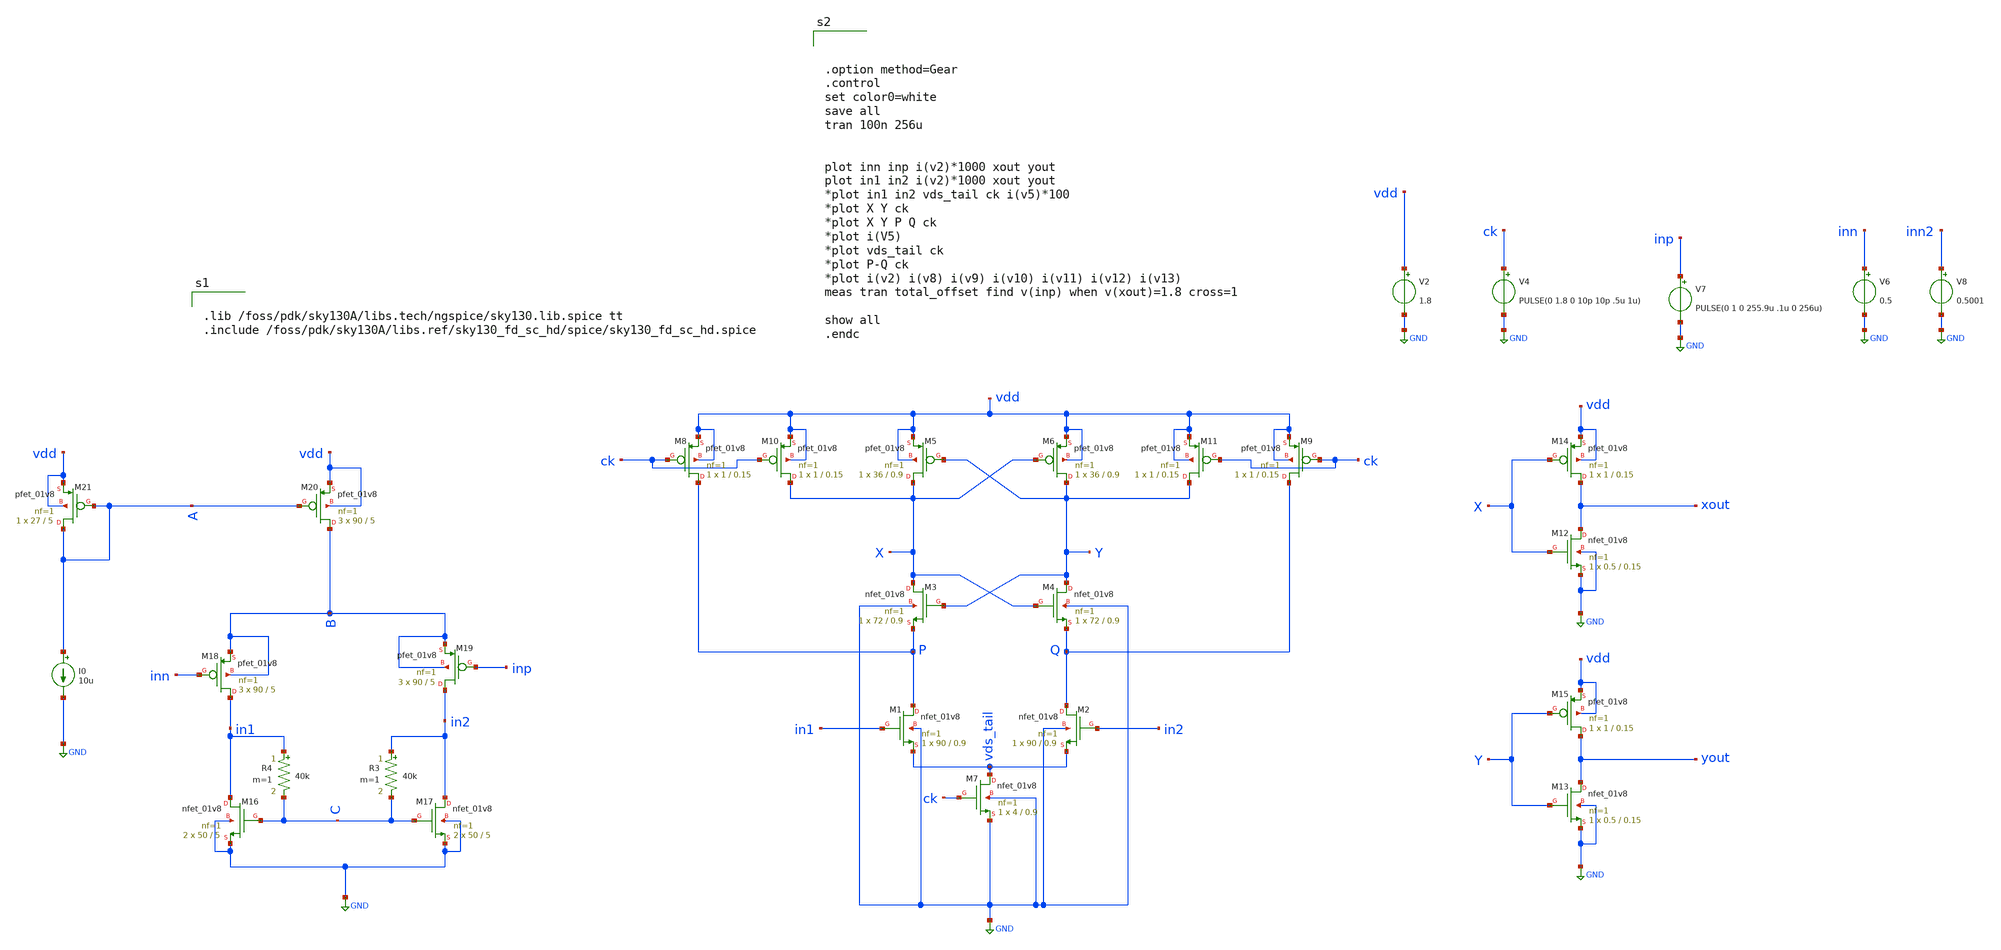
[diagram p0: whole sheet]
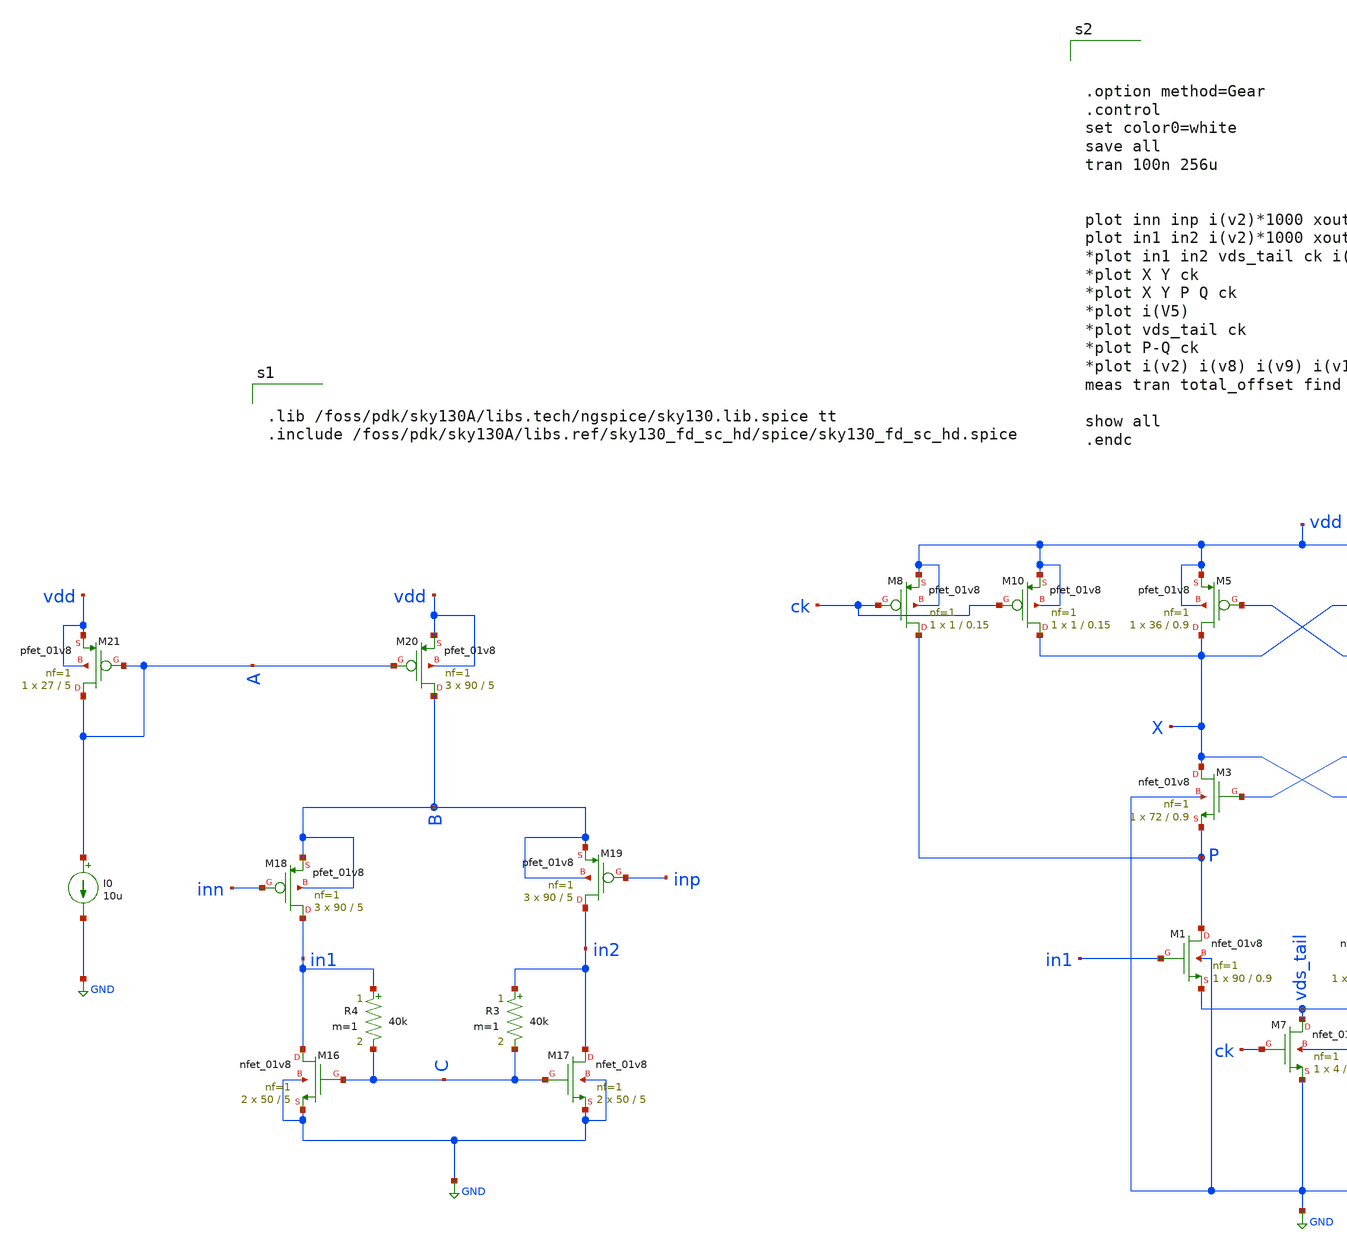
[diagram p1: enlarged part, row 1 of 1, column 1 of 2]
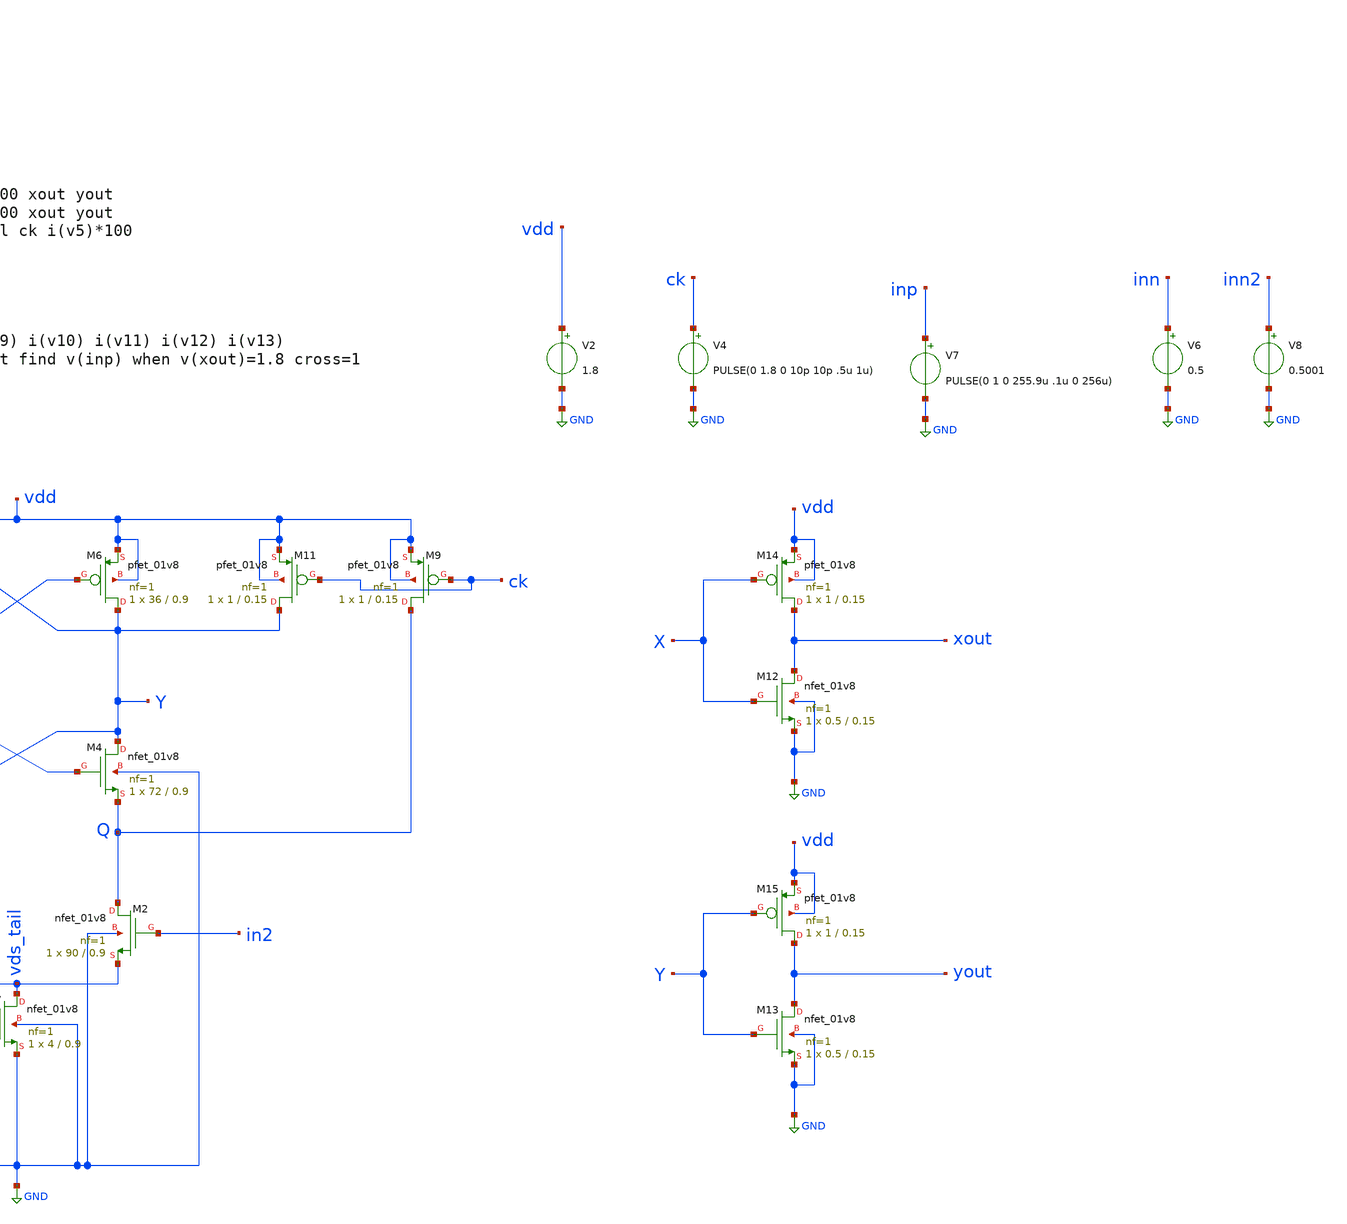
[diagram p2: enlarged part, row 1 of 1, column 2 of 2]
** sch_path: analog/lib/comp_with_preamp_large_new.sch
**.subckt comp_with_preamp_large_new
XM10 X ck vdd vdd sky130_fd_pr__pfet_01v8 L=0.15 W=1 nf=1 ad='int((nf+1)/2) * W/nf * 0.29' as='int((nf+2)/2) * W/nf * 0.29'
+ pd='2*int((nf+1)/2) * (W/nf + 0.29)' ps='2*int((nf+2)/2) * (W/nf + 0.29)' nrd='0.29 / W' nrs='0.29 / W'
+ sa=0 sb=0 sd=0 mult=1 m=1
XM8 P ck vdd vdd sky130_fd_pr__pfet_01v8 L=0.15 W=1 nf=1 ad='int((nf+1)/2) * W/nf * 0.29' as='int((nf+2)/2) * W/nf * 0.29'
+ pd='2*int((nf+1)/2) * (W/nf + 0.29)' ps='2*int((nf+2)/2) * (W/nf + 0.29)' nrd='0.29 / W' nrs='0.29 / W'
+ sa=0 sb=0 sd=0 mult=1 m=1
XM5 X Y vdd vdd sky130_fd_pr__pfet_01v8 L=0.9 W=36 nf=1 ad='int((nf+1)/2) * W/nf * 0.29' as='int((nf+2)/2) * W/nf * 0.29'
+ pd='2*int((nf+1)/2) * (W/nf + 0.29)' ps='2*int((nf+2)/2) * (W/nf + 0.29)' nrd='0.29 / W' nrs='0.29 / W'
+ sa=0 sb=0 sd=0 mult=1 m=1
XM6 Y X vdd vdd sky130_fd_pr__pfet_01v8 L=0.9 W=36 nf=1 ad='int((nf+1)/2) * W/nf * 0.29' as='int((nf+2)/2) * W/nf * 0.29'
+ pd='2*int((nf+1)/2) * (W/nf + 0.29)' ps='2*int((nf+2)/2) * (W/nf + 0.29)' nrd='0.29 / W' nrs='0.29 / W'
+ sa=0 sb=0 sd=0 mult=1 m=1
XM11 Y ck vdd vdd sky130_fd_pr__pfet_01v8 L=0.15 W=1 nf=1 ad='int((nf+1)/2) * W/nf * 0.29' as='int((nf+2)/2) * W/nf * 0.29'
+ pd='2*int((nf+1)/2) * (W/nf + 0.29)' ps='2*int((nf+2)/2) * (W/nf + 0.29)' nrd='0.29 / W' nrs='0.29 / W'
+ sa=0 sb=0 sd=0 mult=1 m=1
XM9 Q ck vdd vdd sky130_fd_pr__pfet_01v8 L=0.15 W=1 nf=1 ad='int((nf+1)/2) * W/nf * 0.29' as='int((nf+2)/2) * W/nf * 0.29'
+ pd='2*int((nf+1)/2) * (W/nf + 0.29)' ps='2*int((nf+2)/2) * (W/nf + 0.29)' nrd='0.29 / W' nrs='0.29 / W'
+ sa=0 sb=0 sd=0 mult=1 m=1
XM3 X Y P GND sky130_fd_pr__nfet_01v8 L=0.9 W=72 nf=1 ad='int((nf+1)/2) * W/nf * 0.29' as='int((nf+2)/2) * W/nf * 0.29'
+ pd='2*int((nf+1)/2) * (W/nf + 0.29)' ps='2*int((nf+2)/2) * (W/nf + 0.29)' nrd='0.29 / W' nrs='0.29 / W'
+ sa=0 sb=0 sd=0 mult=1 m=1
XM4 Y X Q GND sky130_fd_pr__nfet_01v8 L=0.9 W=72 nf=1 ad='int((nf+1)/2) * W/nf * 0.29' as='int((nf+2)/2) * W/nf * 0.29'
+ pd='2*int((nf+1)/2) * (W/nf + 0.29)' ps='2*int((nf+2)/2) * (W/nf + 0.29)' nrd='0.29 / W' nrs='0.29 / W'
+ sa=0 sb=0 sd=0 mult=1 m=1
XM1 P in1 vds_tail GND sky130_fd_pr__nfet_01v8 L=0.9 W=90 nf=1 ad='int((nf+1)/2) * W/nf * 0.29' as='int((nf+2)/2) * W/nf * 0.29'
+ pd='2*int((nf+1)/2) * (W/nf + 0.29)' ps='2*int((nf+2)/2) * (W/nf + 0.29)' nrd='0.29 / W' nrs='0.29 / W'
+ sa=0 sb=0 sd=0 mult=1 m=1
XM2 Q in2 vds_tail GND sky130_fd_pr__nfet_01v8 L=0.9 W=90 nf=1 ad='int((nf+1)/2) * W/nf * 0.29' as='int((nf+2)/2) * W/nf * 0.29'
+ pd='2*int((nf+1)/2) * (W/nf + 0.29)' ps='2*int((nf+2)/2) * (W/nf + 0.29)' nrd='0.29 / W' nrs='0.29 / W'
+ sa=0 sb=0 sd=0 mult=1 m=1
XM7 vds_tail ck GND GND sky130_fd_pr__nfet_01v8 L=0.9 W=4 nf=1 ad='int((nf+1)/2) * W/nf * 0.29' as='int((nf+2)/2) * W/nf * 0.29'
+ pd='2*int((nf+1)/2) * (W/nf + 0.29)' ps='2*int((nf+2)/2) * (W/nf + 0.29)' nrd='0.29 / W' nrs='0.29 / W'
+ sa=0 sb=0 sd=0 mult=1 m=1
XM12 xout X GND GND sky130_fd_pr__nfet_01v8 L=0.15 W=0.5 nf=1 ad='int((nf+1)/2) * W/nf * 0.29' as='int((nf+2)/2) * W/nf * 0.29'
+ pd='2*int((nf+1)/2) * (W/nf + 0.29)' ps='2*int((nf+2)/2) * (W/nf + 0.29)' nrd='0.29 / W' nrs='0.29 / W'
+ sa=0 sb=0 sd=0 mult=1 m=1
XM14 xout X vdd vdd sky130_fd_pr__pfet_01v8 L=0.15 W=1 nf=1 ad='int((nf+1)/2) * W/nf * 0.29' as='int((nf+2)/2) * W/nf * 0.29'
+ pd='2*int((nf+1)/2) * (W/nf + 0.29)' ps='2*int((nf+2)/2) * (W/nf + 0.29)' nrd='0.29 / W' nrs='0.29 / W'
+ sa=0 sb=0 sd=0 mult=1 m=1
XM13 yout Y GND GND sky130_fd_pr__nfet_01v8 L=0.15 W=0.5 nf=1 ad='int((nf+1)/2) * W/nf * 0.29' as='int((nf+2)/2) * W/nf * 0.29'
+ pd='2*int((nf+1)/2) * (W/nf + 0.29)' ps='2*int((nf+2)/2) * (W/nf + 0.29)' nrd='0.29 / W' nrs='0.29 / W'
+ sa=0 sb=0 sd=0 mult=1 m=1
XM15 yout Y vdd vdd sky130_fd_pr__pfet_01v8 L=0.15 W=1 nf=1 ad='int((nf+1)/2) * W/nf * 0.29' as='int((nf+2)/2) * W/nf * 0.29'
+ pd='2*int((nf+1)/2) * (W/nf + 0.29)' ps='2*int((nf+2)/2) * (W/nf + 0.29)' nrd='0.29 / W' nrs='0.29 / W'
+ sa=0 sb=0 sd=0 mult=1 m=1
XM16 in1 C GND GND sky130_fd_pr__nfet_01v8 L=5 W=50 nf=1 ad='int((nf+1)/2) * W/nf * 0.29' as='int((nf+2)/2) * W/nf * 0.29'
+ pd='2*int((nf+1)/2) * (W/nf + 0.29)' ps='2*int((nf+2)/2) * (W/nf + 0.29)' nrd='0.29 / W' nrs='0.29 / W'
+ sa=0 sb=0 sd=0 mult=2 m=2
XM17 in2 C GND GND sky130_fd_pr__nfet_01v8 L=5 W=50 nf=1 ad='int((nf+1)/2) * W/nf * 0.29' as='int((nf+2)/2) * W/nf * 0.29'
+ pd='2*int((nf+1)/2) * (W/nf + 0.29)' ps='2*int((nf+2)/2) * (W/nf + 0.29)' nrd='0.29 / W' nrs='0.29 / W'
+ sa=0 sb=0 sd=0 mult=2 m=2
XM18 in1 inn B B sky130_fd_pr__pfet_01v8 L=5 W=90 nf=1 ad='int((nf+1)/2) * W/nf * 0.29' as='int((nf+2)/2) * W/nf * 0.29'
+ pd='2*int((nf+1)/2) * (W/nf + 0.29)' ps='2*int((nf+2)/2) * (W/nf + 0.29)' nrd='0.29 / W' nrs='0.29 / W'
+ sa=0 sb=0 sd=0 mult=3 m=3
XM19 in2 inp B B sky130_fd_pr__pfet_01v8 L=5 W=90 nf=1 ad='int((nf+1)/2) * W/nf * 0.29' as='int((nf+2)/2) * W/nf * 0.29'
+ pd='2*int((nf+1)/2) * (W/nf + 0.29)' ps='2*int((nf+2)/2) * (W/nf + 0.29)' nrd='0.29 / W' nrs='0.29 / W'
+ sa=0 sb=0 sd=0 mult=3 m=3
R3 in2 C 40k m=1
R4 in1 C 40k m=1
I0 A GND 10u
XM21 A A vdd vdd sky130_fd_pr__pfet_01v8 L=5 W=27 nf=1 ad='int((nf+1)/2) * W/nf * 0.29' as='int((nf+2)/2) * W/nf * 0.29'
+ pd='2*int((nf+1)/2) * (W/nf + 0.29)' ps='2*int((nf+2)/2) * (W/nf + 0.29)' nrd='0.29 / W' nrs='0.29 / W'
+ sa=0 sb=0 sd=0 mult=1 m=1
XM20 B A vdd vdd sky130_fd_pr__pfet_01v8 L=5 W=90 nf=1 ad='int((nf+1)/2) * W/nf * 0.29' as='int((nf+2)/2) * W/nf * 0.29'
+ pd='2*int((nf+1)/2) * (W/nf + 0.29)' ps='2*int((nf+2)/2) * (W/nf + 0.29)' nrd='0.29 / W' nrs='0.29 / W'
+ sa=0 sb=0 sd=0 mult=3 m=3
V2 vdd GND 1.8
V4 ck GND PULSE(0 1.8 0 10p 10p .5u 1u)
V6 inn GND 0.5
V7 inp GND PULSE(0 1 0 255.9u .1u 0 256u)
V8 inn2 GND 0.5001
**** begin user architecture code


.lib /foss/pdk/sky130A/libs.tech/ngspice/sky130.lib.spice tt
.include /foss/pdk/sky130A/libs.ref/sky130_fd_sc_hd/spice/sky130_fd_sc_hd.spice





.option method=Gear
.control
set color0=white
save all
tran 100n 256u


plot inn inp i(v2)*1000 xout yout
plot in1 in2 i(v2)*1000 xout yout
*plot in1 in2 vds_tail ck i(v5)*100
*plot X Y ck
*plot X Y P Q ck
*plot i(V5)
*plot vds_tail ck
*plot P-Q ck
*plot i(v2) i(v8) i(v9) i(v10) i(v11) i(v12) i(v13)
meas tran total_offset find v(inp) when v(xout)=1.8 cross=1

show all
.endc


**** end user architecture code
**.ends
.GLOBAL GND
.end
